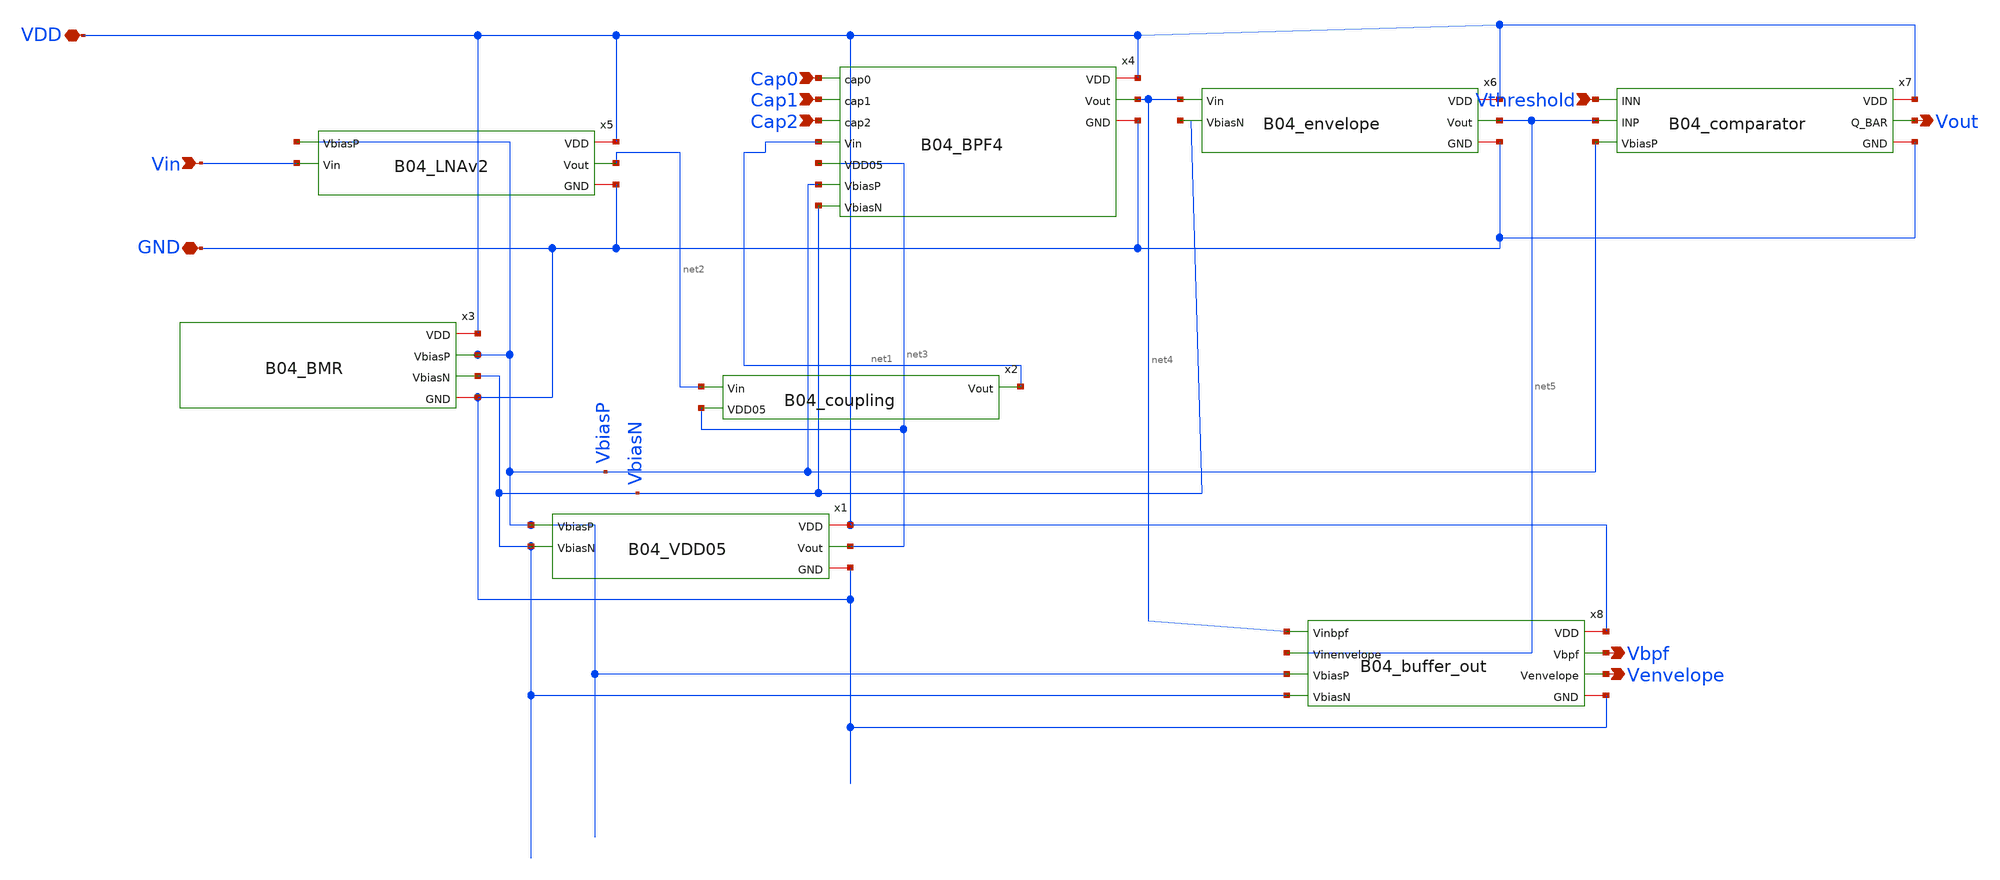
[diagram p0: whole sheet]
** sch_path: analog/B04_AFE_top.sch
**.subckt B04_AFE_top Vin VDD GND Vout Cap0 Cap1 Cap2 Vthreshold Vbpf Venvelope
*.ipin Vin
*.iopin VDD
*.iopin GND
*.opin Vout
*.ipin Cap0
*.ipin Cap1
*.ipin Cap2
*.ipin Vthreshold
*.opin Vbpf
*.opin Venvelope
x5 VDD VbiasP net2 Vin GND B04_LNAv2
x3 VDD VbiasP VbiasN GND B04_BMR
x2 net1 net2 net3 B04_coupling
x1 VDD net3 GND VbiasP VbiasN B04_VDD05
x4 Cap0 Cap1 Cap2 VDD net1 net4 net3 VbiasP VbiasN GND B04_BPF4
x6 VDD net4 net5 VbiasN GND B04_envelope
x7 VDD Vout Vthreshold net5 VbiasP GND B04_comparator
x8 VDD net4 Vbpf net5 Venvelope GND VbiasP VbiasN B04_buffer_out
**.ends
.end
